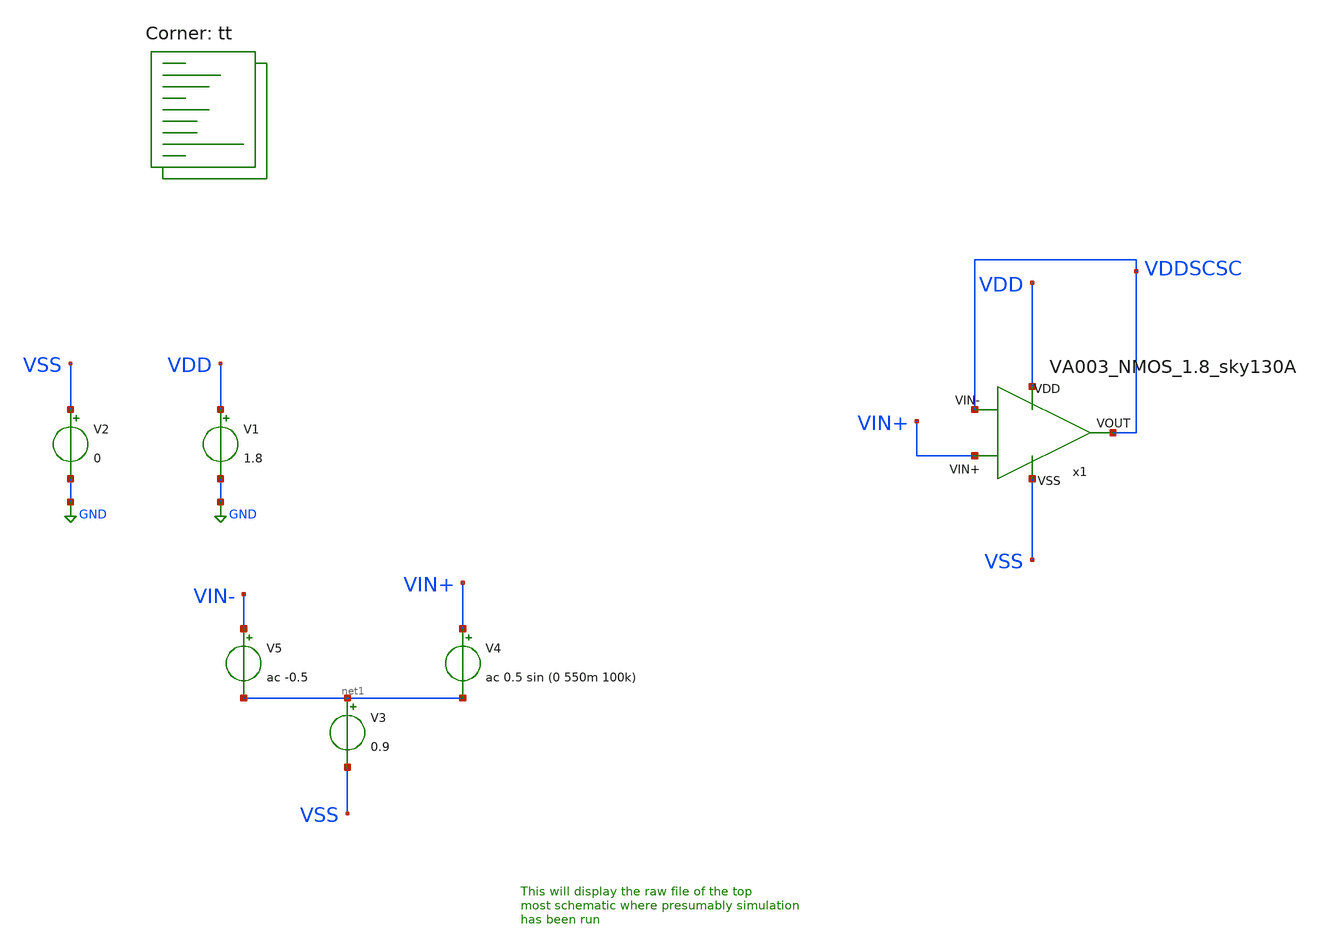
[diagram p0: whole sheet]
** sch_path: my_ip/testbenches_sky/single_ended_OTAS_testbenches/op_tb.sch
**.subckt op_tb
V1 VDD GND 1.8
V2 VSS GND 0
V3 net1 VSS 0.9
V4 VIN+ net1 ac 0.5 sin (0 550m 100k)
V5 VIN- net1 ac -0.5
x1 VDD VSS VDDSCSC VIN+ VDDSCSC VA003_NMOS_1.8_sky130A
**** begin user architecture code
.lib $::SKYWATER_MODELS/sky130.lib.spice tt
**** end user architecture code
**.ends

* expanding   symbol:  VA003_NMOS_1.8_sky130A.sym # of pins=5
** sym_path: my_ip/LIB/Sky130A/single ended amplifiers/VA003_NMOS_1.8_sky130A.sym
** sch_path: my_ip/LIB/Sky130A/single ended amplifiers/VA003_NMOS_1.8_sky130A.sch
.subckt VA003_NMOS_1.8_sky130A VDD VSS VIN- VIN+ VOUT
*.iopin VDD
*.iopin VSS
*.iopin VIN-
*.iopin VIN+
*.iopin VOUT
XR10 VSS net4 VSS sky130_fd_pr__res_xhigh_po_0p35 L=1.2 mult=2 m=2
XM4 net1 net2 net3 VSS sky130_fd_pr__nfet_01v8 L=3 W='2 * 2 ' nf=2 ad='int((2 + 1)/2) * 2 / 2 * 0.29'
+ as='int((2 + 2)/2) * 2 / 2 * 0.29' pd='2*int((2 + 1)/2) * (2 / 2 + 0.29)' ps='2*int((2 + 2)/2) * (2 / 2 + 0.29)'
+ nrd='0.29 / 2 ' nrs='0.29 / 2 ' sa=0 sb=0 sd=0 mult=4 m=4
XM3 net2 net2 V1 VSS sky130_fd_pr__nfet_01v8 L=3 W='2 * 2 ' nf=2 ad='int((2 + 1)/2) * 2 / 2 * 0.29' as='int((2 + 2)/2) * 2 / 2 * 0.29'
+ pd='2*int((2 + 1)/2) * (2 / 2 + 0.29)' ps='2*int((2 + 2)/2) * (2 / 2 + 0.29)' nrd='0.29 / 2 ' nrs='0.29 / 2 '
+ sa=0 sb=0 sd=0 mult=4 m=4
XM6 net3 V1 net4 VSS sky130_fd_pr__nfet_01v8 L=2 W='3 * 2 ' nf=2 ad='int((2 + 1)/2) * 3 / 2 * 0.29' as='int((2 + 2)/2) * 3 / 2 * 0.29'
+ pd='2*int((2 + 1)/2) * (3 / 2 + 0.29)' ps='2*int((2 + 2)/2) * (3 / 2 + 0.29)' nrd='0.29 / 3 ' nrs='0.29 / 3 '
+ sa=0 sb=0 sd=0 mult=8 m=8
XM5 V1 V1 VSS VSS sky130_fd_pr__nfet_01v8 L=2 W='3 * 2 ' nf=2 ad='int((2 + 1)/2) * 3 / 2 * 0.29' as='int((2 + 2)/2) * 3 / 2 * 0.29'
+ pd='2*int((2 + 1)/2) * (3 / 2 + 0.29)' ps='2*int((2 + 2)/2) * (3 / 2 + 0.29)' nrd='0.29 / 3 ' nrs='0.29 / 3 '
+ sa=0 sb=0 sd=0 mult=2 m=2
XM2 net2 net1 VDD VDD sky130_fd_pr__pfet_01v8_lvt L=3 W='4 * 2 ' nf=2 ad='int((2 + 1)/2) * 4 / 2 * 0.29'
+ as='int((2 + 2)/2) * 4 / 2 * 0.29' pd='2*int((2 + 1)/2) * (4 / 2 + 0.29)' ps='2*int((2 + 2)/2) * (4 / 2 + 0.29)'
+ nrd='0.29 / 4 ' nrs='0.29 / 4 ' sa=0 sb=0 sd=0 mult=2 m=2
XM1 net1 net1 VDD VDD sky130_fd_pr__pfet_01v8_lvt L=3 W='4 * 2 ' nf=2 ad='int((2 + 1)/2) * 4 / 2 * 0.29'
+ as='int((2 + 2)/2) * 4 / 2 * 0.29' pd='2*int((2 + 1)/2) * (4 / 2 + 0.29)' ps='2*int((2 + 2)/2) * (4 / 2 + 0.29)'
+ nrd='0.29 / 4 ' nrs='0.29 / 4 ' sa=0 sb=0 sd=0 mult=2 m=2
XM7 net5 V1 VSS VSS sky130_fd_pr__nfet_01v8 L=2 W='3 * 2 ' nf=2 ad='int((2 + 1)/2) * 3 / 2 * 0.29' as='int((2 + 2)/2) * 3 / 2 * 0.29'
+ pd='2*int((2 + 1)/2) * (3 / 2 + 0.29)' ps='2*int((2 + 2)/2) * (3 / 2 + 0.29)' nrd='0.29 / 3 ' nrs='0.29 / 3 '
+ sa=0 sb=0 sd=0 mult=24 m=24
XM34 net6 VIN+ net5 VSS sky130_fd_pr__nfet_01v8 L=1 W='6 * 4 ' nf=4 ad='int((4 + 1)/2) * 6 / 4 * 0.29'
+ as='int((4 + 2)/2) * 6 / 4 * 0.29' pd='2*int((4 + 1)/2) * (6 / 4 + 0.29)' ps='2*int((4 + 2)/2) * (6 / 4 + 0.29)'
+ nrd='0.29 / 6 ' nrs='0.29 / 6 ' sa=0 sb=0 sd=0 mult=4 m=4
XM8 net7 VIN- net5 VSS sky130_fd_pr__nfet_01v8 L=1 W='6 * 4 ' nf=4 ad='int((4 + 1)/2) * 6 / 4 * 0.29'
+ as='int((4 + 2)/2) * 6 / 4 * 0.29' pd='2*int((4 + 1)/2) * (6 / 4 + 0.29)' ps='2*int((4 + 2)/2) * (6 / 4 + 0.29)'
+ nrd='0.29 / 6 ' nrs='0.29 / 6 ' sa=0 sb=0 sd=0 mult=4 m=4
XM9 net6 net6 VDD VDD sky130_fd_pr__pfet_01v8_lvt L=1 W='3 * 2 ' nf=2 ad='int((2 + 1)/2) * 3 / 2 * 0.29'
+ as='int((2 + 2)/2) * 3 / 2 * 0.29' pd='2*int((2 + 1)/2) * (3 / 2 + 0.29)' ps='2*int((2 + 2)/2) * (3 / 2 + 0.29)'
+ nrd='0.29 / 3 ' nrs='0.29 / 3 ' sa=0 sb=0 sd=0 mult=2 m=2
XM10 net7 net6 VDD VDD sky130_fd_pr__pfet_01v8_lvt L=1 W='3 * 2 ' nf=2 ad='int((2 + 1)/2) * 3 / 2 * 0.29'
+ as='int((2 + 2)/2) * 3 / 2 * 0.29' pd='2*int((2 + 1)/2) * (3 / 2 + 0.29)' ps='2*int((2 + 2)/2) * (3 / 2 + 0.29)'
+ nrd='0.29 / 3 ' nrs='0.29 / 3 ' sa=0 sb=0 sd=0 mult=2 m=2
XM11 VB1 V1 VSS VSS sky130_fd_pr__nfet_01v8 L=2 W='3 * 2 ' nf=2 ad='int((2 + 1)/2) * 3 / 2 * 0.29' as='int((2 + 2)/2) * 3 / 2 * 0.29'
+ pd='2*int((2 + 1)/2) * (3 / 2 + 0.29)' ps='2*int((2 + 2)/2) * (3 / 2 + 0.29)' nrd='0.29 / 3 ' nrs='0.29 / 3 '
+ sa=0 sb=0 sd=0 mult=12 m=12
XR32 VB1 VB2 VSS sky130_fd_pr__res_xhigh_po_0p35 L=2 mult=2 m=2
XM13 VB2 VB1 net8 VDD sky130_fd_pr__pfet_01v8_lvt L=1 W='4 * 4 ' nf=4 ad='int((4 + 1)/2) * 4 / 4 * 0.29'
+ as='int((4 + 2)/2) * 4 / 4 * 0.29' pd='2*int((4 + 1)/2) * (4 / 4 + 0.29)' ps='2*int((4 + 2)/2) * (4 / 4 + 0.29)'
+ nrd='0.29 / 4 ' nrs='0.29 / 4 ' sa=0 sb=0 sd=0 mult=2 m=2
XM12 net8 VB2 VDD VDD sky130_fd_pr__pfet_01v8_lvt L=1 W='4 * 4 ' nf=4 ad='int((4 + 1)/2) * 4 / 4 * 0.29'
+ as='int((4 + 2)/2) * 4 / 4 * 0.29' pd='2*int((4 + 1)/2) * (4 / 4 + 0.29)' ps='2*int((4 + 2)/2) * (4 / 4 + 0.29)'
+ nrd='0.29 / 4 ' nrs='0.29 / 4 ' sa=0 sb=0 sd=0 mult=2 m=2
XM14 net9 VB2 VDD VDD sky130_fd_pr__pfet_01v8_lvt L=1 W='4 * 4 ' nf=4 ad='int((4 + 1)/2) * 4 / 4 * 0.29'
+ as='int((4 + 2)/2) * 4 / 4 * 0.29' pd='2*int((4 + 1)/2) * (4 / 4 + 0.29)' ps='2*int((4 + 2)/2) * (4 / 4 + 0.29)'
+ nrd='0.29 / 4 ' nrs='0.29 / 4 ' sa=0 sb=0 sd=0 mult=16 m=16
XM15 net10 VB1 net9 VDD sky130_fd_pr__pfet_01v8_lvt L=1 W='4 * 4 ' nf=4 ad='int((4 + 1)/2) * 4 / 4 * 0.29'
+ as='int((4 + 2)/2) * 4 / 4 * 0.29' pd='2*int((4 + 1)/2) * (4 / 4 + 0.29)' ps='2*int((4 + 2)/2) * (4 / 4 + 0.29)'
+ nrd='0.29 / 4 ' nrs='0.29 / 4 ' sa=0 sb=0 sd=0 mult=16 m=16
XM17 net11 net7 VOUT net10 sky130_fd_pr__pfet_01v8_lvt L=0.35 W='6 * 20 ' nf=20 ad='int((20 + 1)/2) * 6 / 20 * 0.29'
+ as='int((20 + 2)/2) * 6 / 20 * 0.29' pd='2*int((20 + 1)/2) * (6 / 20 + 0.29)' ps='2*int((20 + 2)/2) * (6 / 20 + 0.29)'
+ nrd='0.29 / 6 ' nrs='0.29 / 6 ' sa=0 sb=0 sd=0 mult=4 m=4
XM18 VSS net7 net11 net11 sky130_fd_pr__pfet_01v8_lvt L=0.35 W='6 * 20 ' nf=20 ad='int((20 + 1)/2) * 6 / 20 * 0.29'
+ as='int((20 + 2)/2) * 6 / 20 * 0.29' pd='2*int((20 + 1)/2) * (6 / 20 + 0.29)' ps='2*int((20 + 2)/2) * (6 / 20 + 0.29)'
+ nrd='0.29 / 6 ' nrs='0.29 / 6 ' sa=0 sb=0 sd=0 mult=4 m=4
XM16 VOUT VOUT net10 net10 sky130_fd_pr__pfet_01v8_lvt L=0.35 W='6 * 20 ' nf=20 ad='int((20 + 1)/2) * 6 / 20 * 0.29'
+ as='int((20 + 2)/2) * 6 / 20 * 0.29' pd='2*int((20 + 1)/2) * (6 / 20 + 0.29)' ps='2*int((20 + 2)/2) * (6 / 20 + 0.29)'
+ nrd='0.29 / 6 ' nrs='0.29 / 6 ' sa=0 sb=0 sd=0 mult=4 m=4
XR39 net12 net7 VSS sky130_fd_pr__res_xhigh_po_0p35 L=0.4 mult=2 m=2
XC1 VOUT net12 sky130_fd_pr__cap_mim_m3_2 W=9.6 L=9.6 MF=20 m=20
.ends

.GLOBAL GND
**** begin user architecture code


* ngspice commands
.options savecurrents
.TEMP 27
.control
save all
save @m.x1.xm1.msky130_fd_pr__pfet_01v8_lvt[gm]
save @m.x1.xm1.msky130_fd_pr__pfet_01v8_lvt[vth]
save @m.x1.xm1.msky130_fd_pr__pfet_01v8_lvt[gds]
save @m.x1.xm1.msky130_fd_pr__pfet_01v8_lvt[gmbs]
save @m.x1.xm1.msky130_fd_pr__pfet_01v8_lvt[vds]
save @m.x1.xm1.msky130_fd_pr__pfet_01v8_lvt[vgs]


save @m.x1.xm2.msky130_fd_pr__pfet_01v8_lvt[gm]
save @m.x1.xm2.msky130_fd_pr__pfet_01v8_lvt[vth]
save @m.x1.xm2.msky130_fd_pr__pfet_01v8_lvt[gds]
save @m.x1.xm2.msky130_fd_pr__pfet_01v8_lvt[gmbs]
save @m.x1.xm2.msky130_fd_pr__pfet_01v8_lvt[vds]
save @m.x1.xm2.msky130_fd_pr__pfet_01v8_lvt[vgs]

save @m.x1.xm3.msky130_fd_pr__nfet_01v8[gm]
save @m.x1.xm3.msky130_fd_pr__nfet_01v8[vth]
save @m.x1.xm3.msky130_fd_pr__nfet_01v8[gds]
save @m.x1.xm3.msky130_fd_pr__nfet_01v8[gmbs]
save @m.x1.xm3.msky130_fd_pr__nfet_01v8[vds]
save @m.x1.xm3.msky130_fd_pr__nfet_01v8[vgs]

save @m.x1.xm4.msky130_fd_pr__nfet_01v8[gm]
save @m.x1.xm4.msky130_fd_pr__nfet_01v8[vth]
save @m.x1.xm4.msky130_fd_pr__nfet_01v8[gds]
save @m.x1.xm4.msky130_fd_pr__nfet_01v8[gmbs]
save @m.x1.xm4.msky130_fd_pr__nfet_01v8[vds]
save @m.x1.xm4.msky130_fd_pr__nfet_01v8[vgs]

save @m.x1.xm5.msky130_fd_pr__nfet_01v8[gm]
save @m.x1.xm5.msky130_fd_pr__nfet_01v8[vth]
save @m.x1.xm5.msky130_fd_pr__nfet_01v8[gds]
save @m.x1.xm5.msky130_fd_pr__nfet_01v8[gmbs]
save @m.x1.xm5.msky130_fd_pr__nfet_01v8[vds]
save @m.x1.xm5.msky130_fd_pr__nfet_01v8[vgs]

save @m.x1.xm6.msky130_fd_pr__nfet_01v8[gm]
save @m.x1.xm6.msky130_fd_pr__nfet_01v8[vth]
save @m.x1.xm6.msky130_fd_pr__nfet_01v8[gds]
save @m.x1.xm6.msky130_fd_pr__nfet_01v8[gmbs]
save @m.x1.xm6.msky130_fd_pr__nfet_01v8[vds]
save @m.x1.xm6.msky130_fd_pr__nfet_01v8[vgs]

save @m.x1.xm7.msky130_fd_pr__pfet_01v8_lvt[gm]
save @m.x1.xm7.msky130_fd_pr__pfet_01v8_lvt[vth]
save @m.x1.xm7.msky130_fd_pr__pfet_01v8_lvt[gds]
save @m.x1.xm7.msky130_fd_pr__pfet_01v8_lvt[gmbs]
save @m.x1.xm7.msky130_fd_pr__pfet_01v8_lvt[vds]
save @m.x1.xm7.msky130_fd_pr__pfet_01v8_lvt[vgs]

save @m.x1.xm8.msky130_fd_pr__pfet_01v8_lvt[gm]
save @m.x1.xm8.msky130_fd_pr__pfet_01v8_lvt[vth]
save @m.x1.xm8.msky130_fd_pr__pfet_01v8_lvt[gds]
save @m.x1.xm8.msky130_fd_pr__pfet_01v8_lvt[gmbs]
save @m.x1.xm8.msky130_fd_pr__pfet_01v8_lvt[vds]
save @m.x1.xm8.msky130_fd_pr__pfet_01v8_lvt[vgs]

save @m.x1.xm9.msky130_fd_pr__pfet_01v8_lvt[gm]
save @m.x1.xm9.msky130_fd_pr__pfet_01v8_lvt[vth]
save @m.x1.xm9.msky130_fd_pr__pfet_01v8_lvt[gds]
save @m.x1.xm9.msky130_fd_pr__pfet_01v8_lvt[gmbs]
save @m.x1.xm9.msky130_fd_pr__pfet_01v8_lvt[vds]
save @m.x1.xm9.msky130_fd_pr__pfet_01v8_lvt[vgs]


save @m.x1.xm10.msky130_fd_pr__nfet_01v8[gm]
save @m.x1.xm10.msky130_fd_pr__nfet_01v8[vth]
save @m.x1.xm10.msky130_fd_pr__nfet_01v8[gds]
save @m.x1.xm10.msky130_fd_pr__nfet_01v8[gmbs]
save @m.x1.xm10.msky130_fd_pr__nfet_01v8[vds]
save @m.x1.xm10.msky130_fd_pr__nfet_01v8[vgs]


save @m.x1.xm11.msky130_fd_pr__nfet_01v8[gm]
save @m.x1.xm11.msky130_fd_pr__nfet_01v8[vth]
save @m.x1.xm11.msky130_fd_pr__nfet_01v8[gds]
save @m.x1.xm11.msky130_fd_pr__nfet_01v8[gmbs]
save @m.x1.xm11.msky130_fd_pr__nfet_01v8[vds]
save @m.x1.xm11.msky130_fd_pr__nfet_01v8[vgs]

save @m.x1.xm12.msky130_fd_pr__pfet_01v8_lvt[gm]
save @m.x1.xm12.msky130_fd_pr__pfet_01v8_lvt[vth]
save @m.x1.xm12.msky130_fd_pr__pfet_01v8_lvt[gds]
save @m.x1.xm12.msky130_fd_pr__pfet_01v8_lvt[gmbs]
save @m.x1.xm12.msky130_fd_pr__pfet_01v8_lvt[vds]
save @m.x1.xm12.msky130_fd_pr__pfet_01v8_lvt[vgs]

save @m.x1.xm13.msky130_fd_pr__pfet_01v8_lvt[gm]
save @m.x1.xm13.msky130_fd_pr__pfet_01v8_lvt[vth]
save @m.x1.xm13.msky130_fd_pr__pfet_01v8_lvt[gds]
save @m.x1.xm13.msky130_fd_pr__pfet_01v8_lvt[gmbs]
save @m.x1.xm13.msky130_fd_pr__pfet_01v8_lvt[vds]
save @m.x1.xm13.msky130_fd_pr__pfet_01v8_lvt[vgs]




op
write op_tb.raw
dc V3 0 1.8 0.0001
plot v(VDDSCSC)


.endc



**** end user architecture code
.end
